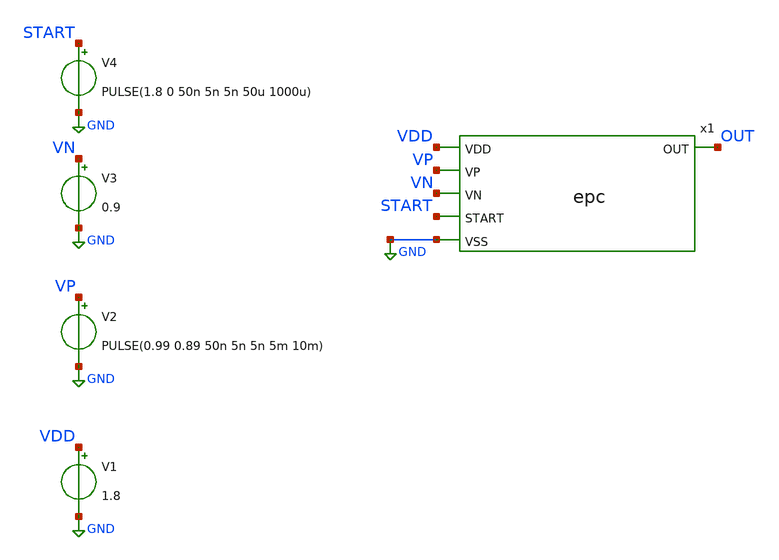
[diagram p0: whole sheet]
** sch_path: xschem/epc_tb.sch
**.subckt epc_tb
x1 VDD VP OUT VN START GND epc
V1 VDD GND 1.8
V2 VP GND PULSE(0.99 0.89 50n 5n 5n 5m 10m)
V3 VN GND 0.9
V4 START GND PULSE(1.8 0 50n 5n 5n 50u 1000u)
**** begin user architecture code

** opencircuitdesign pdks install
.lib $::SKYWATER_MODELS/sky130.lib.spice tt
.include /usr/local/share/pdk/sky130A/libs.ref/sky130_fd_sc_hd/spice/sky130_fd_sc_hd.spice



.option wnflag=0
.option savecurrents
.control
tran 1m 10m
plot V(vp) V(vn) V(out)
.endc

**** end user architecture code
**.ends
.GLOBAL GND
.end
